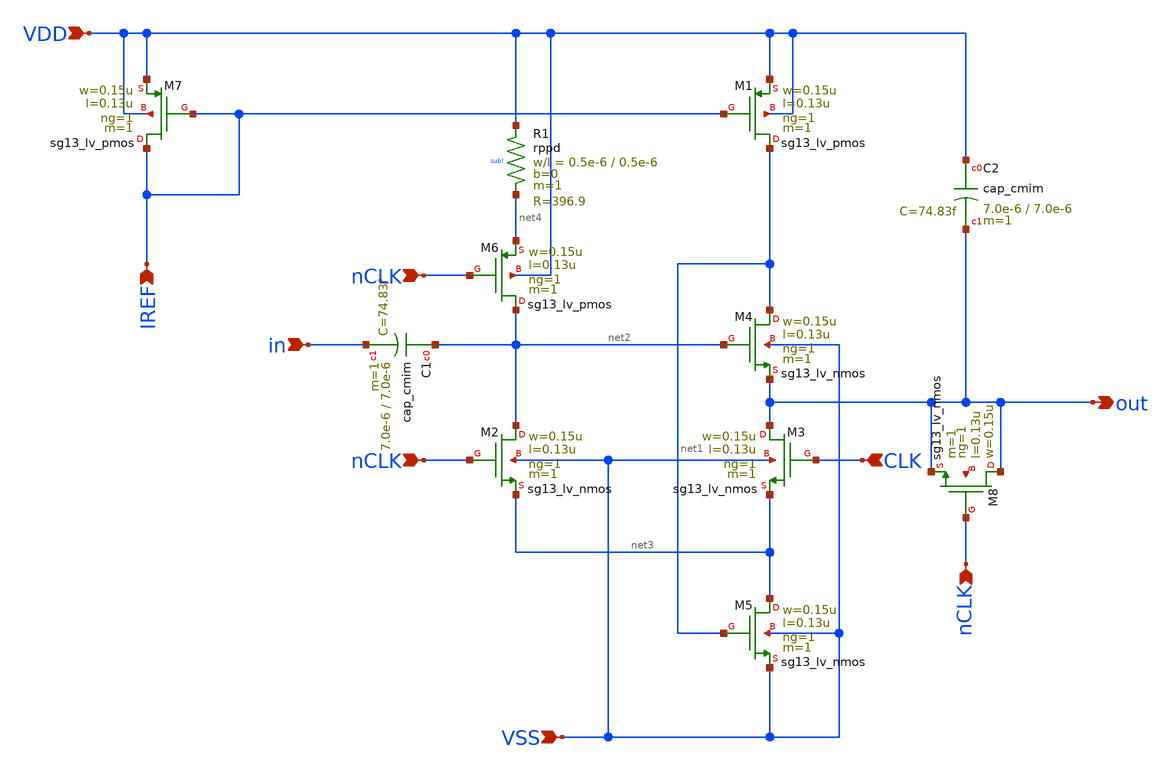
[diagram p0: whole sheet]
** sch_path: UWBPulseGenerator/design_data/xschem/track_hold.sch
**.subckt track_hold IREF out CLK nCLK nCLK nCLK in VDD VSS
*.ipin IREF
*.opin out
*.ipin CLK
*.ipin nCLK
*.ipin nCLK
*.ipin nCLK
*.ipin in
*.ipin VDD
*.ipin VSS
XM1 net1 IREF VDD VDD sg13_lv_pmos w=0.15u l=0.13u ng=1 m=1 mm_ok=1
XM2 net2 nCLK net3 VSS sg13_lv_nmos w=0.15u l=0.13u ng=1 m=1 mm_ok=1
XM3 out CLK net3 VSS sg13_lv_nmos w=0.15u l=0.13u ng=1 m=1 mm_ok=1
XM4 net1 net2 out VSS sg13_lv_nmos w=0.15u l=0.13u ng=1 m=1 mm_ok=1
XM5 net3 net1 VSS VSS sg13_lv_nmos w=0.15u l=0.13u ng=1 m=1 mm_ok=1
XM6 net2 nCLK net4 VDD sg13_lv_pmos w=0.15u l=0.13u ng=1 m=1 mm_ok=1
XC1 net2 in cap_cmim w=7.0e-6 l=7.0e-6 m=1 mm_ok=1
XR1 VDD net4 sub! rppd w=0.5e-6 l=0.5e-6 m=1 b=0 mm_ok=1
XC2 VDD out cap_cmim w=7.0e-6 l=7.0e-6 m=1 mm_ok=1
XM7 IREF IREF VDD VDD sg13_lv_pmos w=0.15u l=0.13u ng=1 m=1 mm_ok=1
XM8 out nCLK out net5 sg13_lv_nmos w=0.15u l=0.13u ng=1 m=1 mm_ok=1
**.ends
.end
